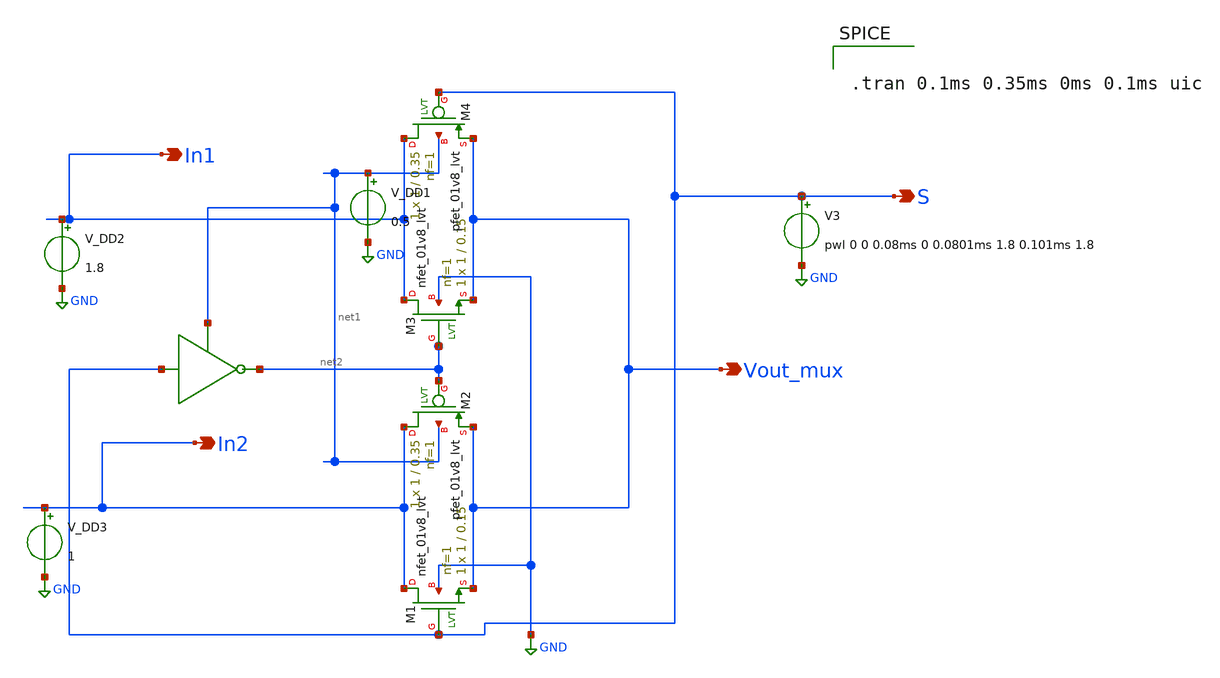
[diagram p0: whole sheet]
** sch_path: Current Sensor/untitled-9.sch
**.subckt untitled-9 Vout_mux S In1 In2
*.opin Vout_mux
*.opin S
*.opin In1
*.opin In2
XM1 In2 S Vout_mux GND sky130_fd_pr__nfet_01v8_lvt L=0.15 W=1 nf=1 ad='int((nf+1)/2) * W/nf * 0.29' as='int((nf+2)/2) * W/nf * 0.29'
+ pd='2*int((nf+1)/2) * (W/nf + 0.29)' ps='2*int((nf+2)/2) * (W/nf + 0.29)' nrd='0.29 / W' nrs='0.29 / W'
+ sa=0 sb=0 sd=0 mult=1 m=1
XM2 In2 net2 Vout_mux net1 sky130_fd_pr__pfet_01v8_lvt L=0.35 W=1 nf=1 ad='int((nf+1)/2) * W/nf * 0.29'
+ as='int((nf+2)/2) * W/nf * 0.29' pd='2*int((nf+1)/2) * (W/nf + 0.29)' ps='2*int((nf+2)/2) * (W/nf + 0.29)'
+ nrd='0.29 / W' nrs='0.29 / W' sa=0 sb=0 sd=0 mult=1 m=1
XM3 In1 net2 Vout_mux GND sky130_fd_pr__nfet_01v8_lvt L=0.15 W=1 nf=1 ad='int((nf+1)/2) * W/nf * 0.29'
+ as='int((nf+2)/2) * W/nf * 0.29' pd='2*int((nf+1)/2) * (W/nf + 0.29)' ps='2*int((nf+2)/2) * (W/nf + 0.29)'
+ nrd='0.29 / W' nrs='0.29 / W' sa=0 sb=0 sd=0 mult=1 m=1
XM4 In1 S Vout_mux net1 sky130_fd_pr__pfet_01v8_lvt L=0.35 W=1 nf=1 ad='int((nf+1)/2) * W/nf * 0.29'
+ as='int((nf+2)/2) * W/nf * 0.29' pd='2*int((nf+1)/2) * (W/nf + 0.29)' ps='2*int((nf+2)/2) * (W/nf + 0.29)'
+ nrd='0.29 / W' nrs='0.29 / W' sa=0 sb=0 sd=0 mult=1 m=1
V3 S GND pwl 0 0 0.08ms 0 0.0801ms 1.8 0.101ms 1.8
V_DD1 net1 GND 0.5
V_DD2 In1 GND 1.8
V_DD3 In2 GND 1
**** begin user architecture code

** opencircuitdesign pdks install
.lib $::SKYWATER_MODELS/sky130.lib.spice tt_mm




.tran 0.1ms 0.35ms 0ms 0.1ms uic

**** end user architecture code
**.ends
.GLOBAL GND
.end
